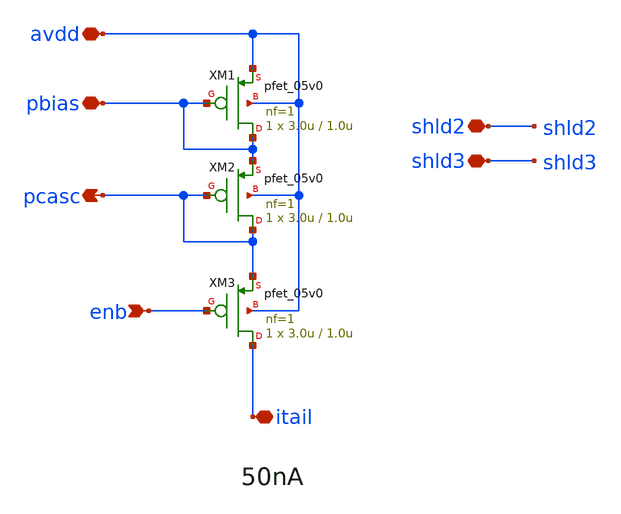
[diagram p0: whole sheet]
** sch_path: projects/programmable_transceiver_platform/analog/core_support/biasgen/xschem/bias_pset2.sch
**.subckt bias_pset2 pbias itail enb pcasc avdd shld2 shld3
*.iopin pbias
*.iopin itail
*.ipin enb
*.opin pcasc
*.iopin avdd
*.iopin shld2
*.iopin shld3
XM1 pbias pbias avdd avdd pfet_05v0 L=1.0u W=3.0u nf=1 ad='int((nf+1)/2) * W/nf * 0.18u' as='int((nf+2)/2) * W/nf * 0.18u'
+ pd='2*int((nf+1)/2) * (W/nf + 0.18u)' ps='2*int((nf+2)/2) * (W/nf + 0.18u)' nrd='0.18u / W' nrs='0.18u / W'
+ sa=0 sb=0 sd=0 m=1 par=1
XM2 pcasc pcasc pbias avdd pfet_05v0 L=1.0u W=3.0u nf=1 ad='int((nf+1)/2) * W/nf * 0.18u' as='int((nf+2)/2) * W/nf * 0.18u'
+ pd='2*int((nf+1)/2) * (W/nf + 0.18u)' ps='2*int((nf+2)/2) * (W/nf + 0.18u)' nrd='0.18u / W' nrs='0.18u / W'
+ sa=0 sb=0 sd=0 m=1 par=1
XM3 itail enb pcasc avdd pfet_05v0 L=1.0u W=3.0u nf=1 ad='int((nf+1)/2) * W/nf * 0.18u' as='int((nf+2)/2) * W/nf * 0.18u'
+ pd='2*int((nf+1)/2) * (W/nf + 0.18u)' ps='2*int((nf+2)/2) * (W/nf + 0.18u)' nrd='0.18u / W' nrs='0.18u / W'
+ sa=0 sb=0 sd=0 m=1 par=1
**.ends
.end
